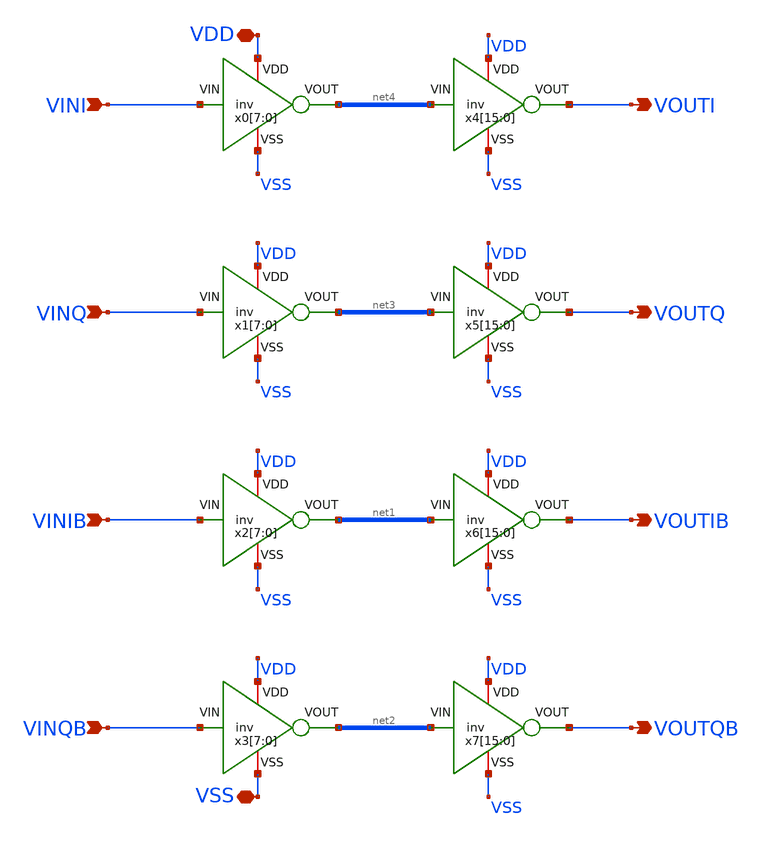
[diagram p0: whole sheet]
** sch_path: 4to4.sch
**.subckt 4to4 VDD VSS VINI VINQ VINIB VINQB VOUTI VOUTQ VOUTIB VOUTQB
*.iopin VDD
*.iopin VSS
*.ipin VINI
*.ipin VINQ
*.ipin VINIB
*.ipin VINQB
*.opin VOUTI
*.opin VOUTQ
*.opin VOUTIB
*.opin VOUTQB
x0[7] VDD net4[7] VINI VSS inv
x0[6] VDD net4[6] VINI VSS inv
x0[5] VDD net4[5] VINI VSS inv
x0[4] VDD net4[4] VINI VSS inv
x0[3] VDD net4[3] VINI VSS inv
x0[2] VDD net4[2] VINI VSS inv
x0[1] VDD net4[1] VINI VSS inv
x0[0] VDD net4[0] VINI VSS inv
x1[7] VDD net3[7] VINQ VSS inv
x1[6] VDD net3[6] VINQ VSS inv
x1[5] VDD net3[5] VINQ VSS inv
x1[4] VDD net3[4] VINQ VSS inv
x1[3] VDD net3[3] VINQ VSS inv
x1[2] VDD net3[2] VINQ VSS inv
x1[1] VDD net3[1] VINQ VSS inv
x1[0] VDD net3[0] VINQ VSS inv
x2[7] VDD net1[7] VINIB VSS inv
x2[6] VDD net1[6] VINIB VSS inv
x2[5] VDD net1[5] VINIB VSS inv
x2[4] VDD net1[4] VINIB VSS inv
x2[3] VDD net1[3] VINIB VSS inv
x2[2] VDD net1[2] VINIB VSS inv
x2[1] VDD net1[1] VINIB VSS inv
x2[0] VDD net1[0] VINIB VSS inv
x3[7] VDD net2[7] VINQB VSS inv
x3[6] VDD net2[6] VINQB VSS inv
x3[5] VDD net2[5] VINQB VSS inv
x3[4] VDD net2[4] VINQB VSS inv
x3[3] VDD net2[3] VINQB VSS inv
x3[2] VDD net2[2] VINQB VSS inv
x3[1] VDD net2[1] VINQB VSS inv
x3[0] VDD net2[0] VINQB VSS inv
x4[15] VDD VOUTI net4[7] VSS inv
x4[14] VDD VOUTI net4[6] VSS inv
x4[13] VDD VOUTI net4[5] VSS inv
x4[12] VDD VOUTI net4[4] VSS inv
x4[11] VDD VOUTI net4[3] VSS inv
x4[10] VDD VOUTI net4[2] VSS inv
x4[9] VDD VOUTI net4[1] VSS inv
x4[8] VDD VOUTI net4[0] VSS inv
x4[7] VDD VOUTI net4[7] VSS inv
x4[6] VDD VOUTI net4[6] VSS inv
x4[5] VDD VOUTI net4[5] VSS inv
x4[4] VDD VOUTI net4[4] VSS inv
x4[3] VDD VOUTI net4[3] VSS inv
x4[2] VDD VOUTI net4[2] VSS inv
x4[1] VDD VOUTI net4[1] VSS inv
x4[0] VDD VOUTI net4[0] VSS inv
x5[15] VDD VOUTQ net3[7] VSS inv
x5[14] VDD VOUTQ net3[6] VSS inv
x5[13] VDD VOUTQ net3[5] VSS inv
x5[12] VDD VOUTQ net3[4] VSS inv
x5[11] VDD VOUTQ net3[3] VSS inv
x5[10] VDD VOUTQ net3[2] VSS inv
x5[9] VDD VOUTQ net3[1] VSS inv
x5[8] VDD VOUTQ net3[0] VSS inv
x5[7] VDD VOUTQ net3[7] VSS inv
x5[6] VDD VOUTQ net3[6] VSS inv
x5[5] VDD VOUTQ net3[5] VSS inv
x5[4] VDD VOUTQ net3[4] VSS inv
x5[3] VDD VOUTQ net3[3] VSS inv
x5[2] VDD VOUTQ net3[2] VSS inv
x5[1] VDD VOUTQ net3[1] VSS inv
x5[0] VDD VOUTQ net3[0] VSS inv
x6[15] VDD VOUTIB net1[7] VSS inv
x6[14] VDD VOUTIB net1[6] VSS inv
x6[13] VDD VOUTIB net1[5] VSS inv
x6[12] VDD VOUTIB net1[4] VSS inv
x6[11] VDD VOUTIB net1[3] VSS inv
x6[10] VDD VOUTIB net1[2] VSS inv
x6[9] VDD VOUTIB net1[1] VSS inv
x6[8] VDD VOUTIB net1[0] VSS inv
x6[7] VDD VOUTIB net1[7] VSS inv
x6[6] VDD VOUTIB net1[6] VSS inv
x6[5] VDD VOUTIB net1[5] VSS inv
x6[4] VDD VOUTIB net1[4] VSS inv
x6[3] VDD VOUTIB net1[3] VSS inv
x6[2] VDD VOUTIB net1[2] VSS inv
x6[1] VDD VOUTIB net1[1] VSS inv
x6[0] VDD VOUTIB net1[0] VSS inv
x7[15] VDD VOUTQB net2[7] VSS inv
x7[14] VDD VOUTQB net2[6] VSS inv
x7[13] VDD VOUTQB net2[5] VSS inv
x7[12] VDD VOUTQB net2[4] VSS inv
x7[11] VDD VOUTQB net2[3] VSS inv
x7[10] VDD VOUTQB net2[2] VSS inv
x7[9] VDD VOUTQB net2[1] VSS inv
x7[8] VDD VOUTQB net2[0] VSS inv
x7[7] VDD VOUTQB net2[7] VSS inv
x7[6] VDD VOUTQB net2[6] VSS inv
x7[5] VDD VOUTQB net2[5] VSS inv
x7[4] VDD VOUTQB net2[4] VSS inv
x7[3] VDD VOUTQB net2[3] VSS inv
x7[2] VDD VOUTQB net2[2] VSS inv
x7[1] VDD VOUTQB net2[1] VSS inv
x7[0] VDD VOUTQB net2[0] VSS inv
**.ends
.end
